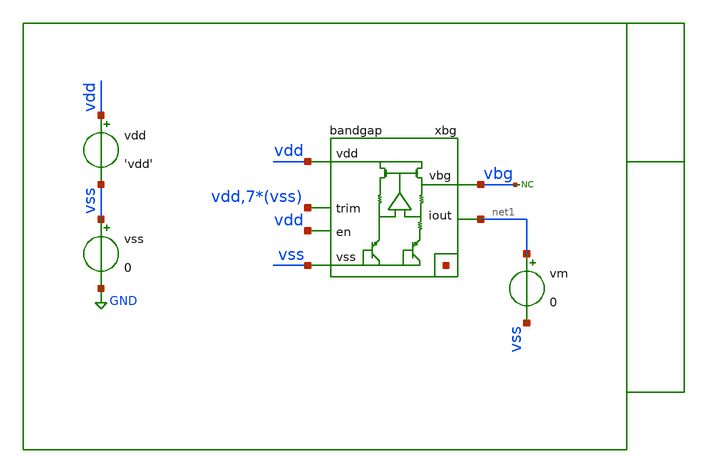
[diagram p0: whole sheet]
** sch_path: xschem/tb/bandgap_cm/bandgap/mm_bandgap_temperature.sch
**.subckt mm_bandgap_temperature
xbg vdd vbg vss net2[7] net2[6] net2[5] net2[4] net2[3] net2[2] net2[1] net2[0] vdd vss vss vss vss
+ vss vss vss net1 vdd bandgap
vdd vdd vss 'vdd'
vss vss GND 0
* noconn vbg
vm net1 vss 0
**** begin user architecture code

* Control

.param vdd = 3.3
.temp 27
.options reltol = 1e-6
.options seedinfo = 1

*------------------------------------------------------------
* Nodeset for better convergence
*------------------------------------------------------------
.nodeset v(vbg)      = '1'
.nodeset v(xbg.gate) = 'vdd/2'
.nodeset v(xbg.vx)   = '0.70'
.nodeset v(xbg.vbe2) = '0.65'
.nodeset v(xbg.vs1)  = '0'
*------------------------------------------------------------

.param nseed = 1
.csparam ns = nseed

.control

alterparam sw_stat_global   = 1
alterparam sw_stat_mismatch = 1
reset

save all

setseed $&ns

dc temp -40 85 5

meas dc vbg_min min vbg from=-40 to=85
meas dc vbg_max max vbg from=-40 to=85

let vbg_min_eval = vbg_min + 1u
let vbg_max_eval = vbg_max - 1u

meas dc t_max when v(vbg)=vbg_max_eval
meas dc t_min when v(vbg)=vbg_min_eval

let dv_dT = (vbg_max-vbg_min)/abs((t_max-t_min))

let iout = abs(vm#branch)

print vbg_min
print vbg_max
print t_min
print t_max
print dv_dT

set wr_singlescale
set wr_vecnames
wrdata data.csv vbg

.endc
.end


 * Model Corners

.include $::CORNERS/ngspice/tt.spice
*.include $::CORNERS/ngspice/ff.spice
*.include $::CORNERS/ngspice/ss.spice
*.include $::CORNERS/ngspice/sf.spice
*.include $::CORNERS/ngspice/fs.spice

**** end user architecture code
**.ends
.GLOBAL GND
.end
